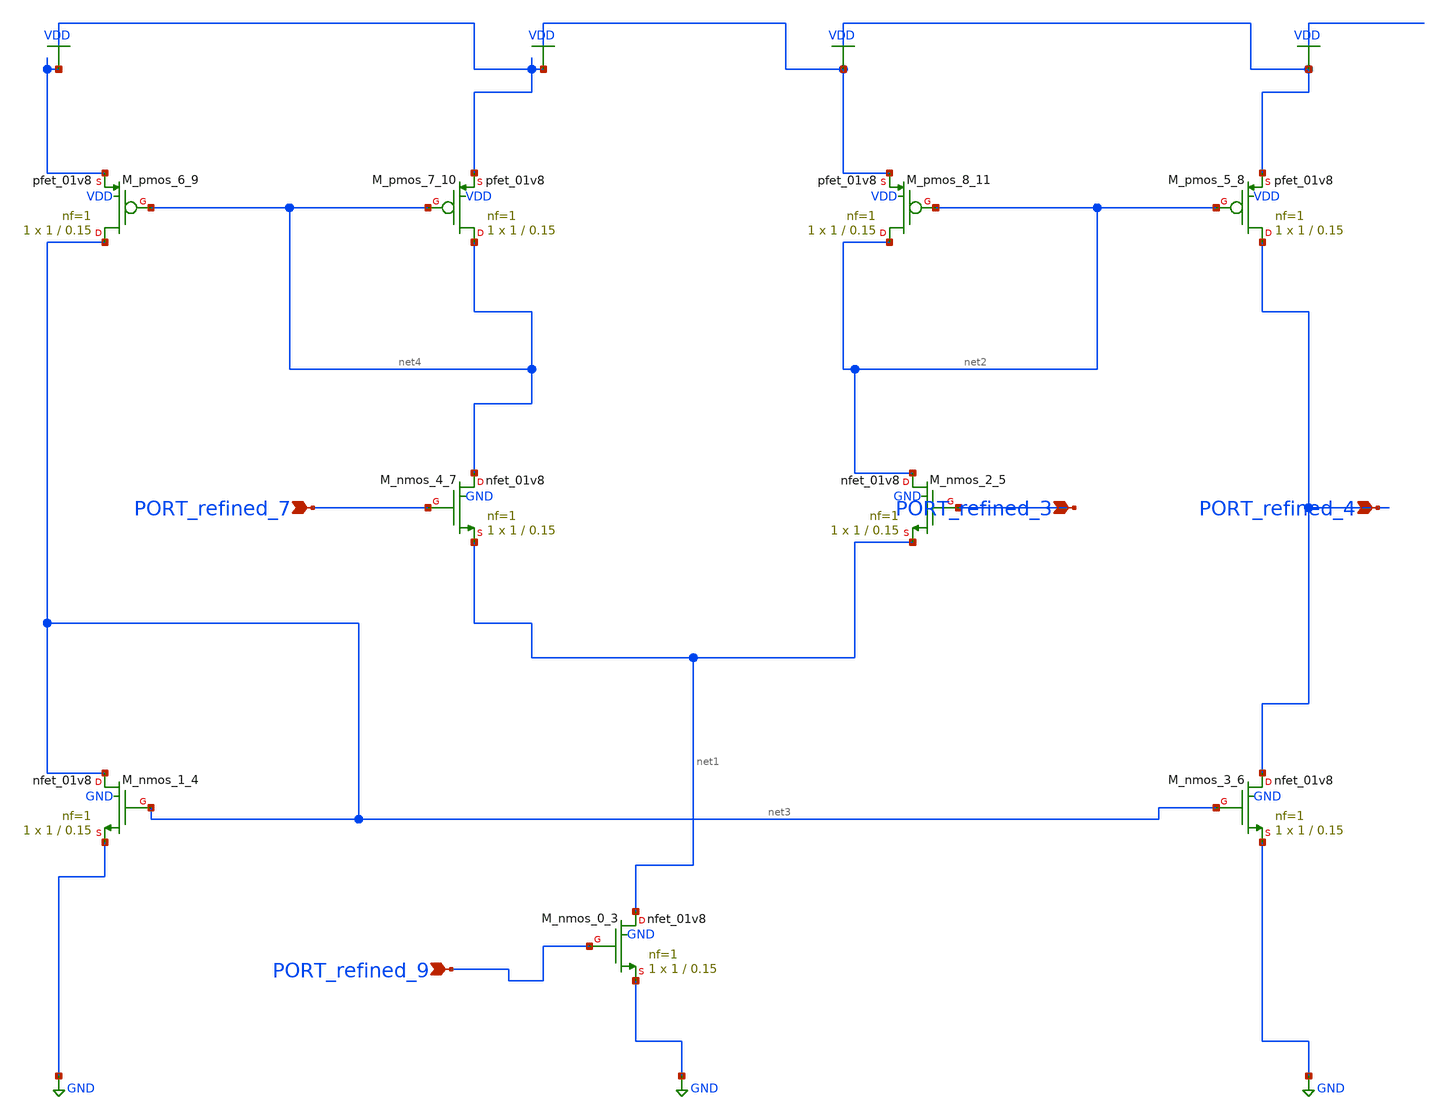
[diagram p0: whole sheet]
** sch_path: schematics/10_1587_elex_17_20200238_03_003_crop1.sch
**.subckt 10_1587_elex_17_20200238_03_003_crop1 PORT_refined_4 PORT_refined_9 PORT_refined_3
*+ PORT_refined_7
*.ipin PORT_refined_4
*.ipin PORT_refined_9
*.ipin PORT_refined_3
*.ipin PORT_refined_7
XM_nmos_0_3 net1 PORT_refined_9 GND GND sky130_fd_pr__nfet_01v8 L=0.15 W=1 nf=1 ad='int((1 + 1)/2) * 1 / 1 * 0.29'
+ as='int((1 + 2)/2) * 1 / 1 * 0.29' pd='2*int((1 + 1)/2) * (1 / 1 + 0.29)' ps='2*int((1 + 2)/2) * (1 / 1 + 0.29)'
+ nrd='0.29 / 1 ' nrs='0.29 / 1 ' sa=0 sb=0 sd=0 mult=1 m=1
XM_nmos_1_4 net3 net3 GND GND sky130_fd_pr__nfet_01v8 L=0.15 W=1 nf=1 ad='int((1 + 1)/2) * 1 / 1 * 0.29'
+ as='int((1 + 2)/2) * 1 / 1 * 0.29' pd='2*int((1 + 1)/2) * (1 / 1 + 0.29)' ps='2*int((1 + 2)/2) * (1 / 1 + 0.29)'
+ nrd='0.29 / 1 ' nrs='0.29 / 1 ' sa=0 sb=0 sd=0 mult=1 m=1
XM_nmos_2_5 net2 PORT_refined_3 net1 GND sky130_fd_pr__nfet_01v8 L=0.15 W=1 nf=1 ad='int((1 + 1)/2) * 1 / 1 * 0.29'
+ as='int((1 + 2)/2) * 1 / 1 * 0.29' pd='2*int((1 + 1)/2) * (1 / 1 + 0.29)' ps='2*int((1 + 2)/2) * (1 / 1 + 0.29)'
+ nrd='0.29 / 1 ' nrs='0.29 / 1 ' sa=0 sb=0 sd=0 mult=1 m=1
XM_nmos_3_6 PORT_refined_4 net3 GND GND sky130_fd_pr__nfet_01v8 L=0.15 W=1 nf=1 ad='int((1 + 1)/2) * 1 / 1 * 0.29'
+ as='int((1 + 2)/2) * 1 / 1 * 0.29' pd='2*int((1 + 1)/2) * (1 / 1 + 0.29)' ps='2*int((1 + 2)/2) * (1 / 1 + 0.29)'
+ nrd='0.29 / 1 ' nrs='0.29 / 1 ' sa=0 sb=0 sd=0 mult=1 m=1
XM_nmos_4_7 net4 PORT_refined_7 net1 GND sky130_fd_pr__nfet_01v8 L=0.15 W=1 nf=1 ad='int((1 + 1)/2) * 1 / 1 * 0.29'
+ as='int((1 + 2)/2) * 1 / 1 * 0.29' pd='2*int((1 + 1)/2) * (1 / 1 + 0.29)' ps='2*int((1 + 2)/2) * (1 / 1 + 0.29)'
+ nrd='0.29 / 1 ' nrs='0.29 / 1 ' sa=0 sb=0 sd=0 mult=1 m=1
XM_pmos_5_8 PORT_refined_4 net2 VDD VDD sky130_fd_pr__pfet_01v8 L=0.15 W=1 nf=1 ad='int((1 + 1)/2) * 1 / 1 * 0.29'
+ as='int((1 + 2)/2) * 1 / 1 * 0.29' pd='2*int((1 + 1)/2) * (1 / 1 + 0.29)' ps='2*int((1 + 2)/2) * (1 / 1 + 0.29)'
+ nrd='0.29 / 1 ' nrs='0.29 / 1 ' sa=0 sb=0 sd=0 mult=1 m=1
XM_pmos_6_9 net3 net4 VDD VDD sky130_fd_pr__pfet_01v8 L=0.15 W=1 nf=1 ad='int((1 + 1)/2) * 1 / 1 * 0.29'
+ as='int((1 + 2)/2) * 1 / 1 * 0.29' pd='2*int((1 + 1)/2) * (1 / 1 + 0.29)' ps='2*int((1 + 2)/2) * (1 / 1 + 0.29)'
+ nrd='0.29 / 1 ' nrs='0.29 / 1 ' sa=0 sb=0 sd=0 mult=1 m=1
XM_pmos_7_10 net4 net4 VDD VDD sky130_fd_pr__pfet_01v8 L=0.15 W=1 nf=1 ad='int((1 + 1)/2) * 1 / 1 * 0.29'
+ as='int((1 + 2)/2) * 1 / 1 * 0.29' pd='2*int((1 + 1)/2) * (1 / 1 + 0.29)' ps='2*int((1 + 2)/2) * (1 / 1 + 0.29)'
+ nrd='0.29 / 1 ' nrs='0.29 / 1 ' sa=0 sb=0 sd=0 mult=1 m=1
XM_pmos_8_11 net2 net2 VDD VDD sky130_fd_pr__pfet_01v8 L=0.15 W=1 nf=1 ad='int((1 + 1)/2) * 1 / 1 * 0.29'
+ as='int((1 + 2)/2) * 1 / 1 * 0.29' pd='2*int((1 + 1)/2) * (1 / 1 + 0.29)' ps='2*int((1 + 2)/2) * (1 / 1 + 0.29)'
+ nrd='0.29 / 1 ' nrs='0.29 / 1 ' sa=0 sb=0 sd=0 mult=1 m=1
**.ends
.GLOBAL GND
.GLOBAL VDD
.end
